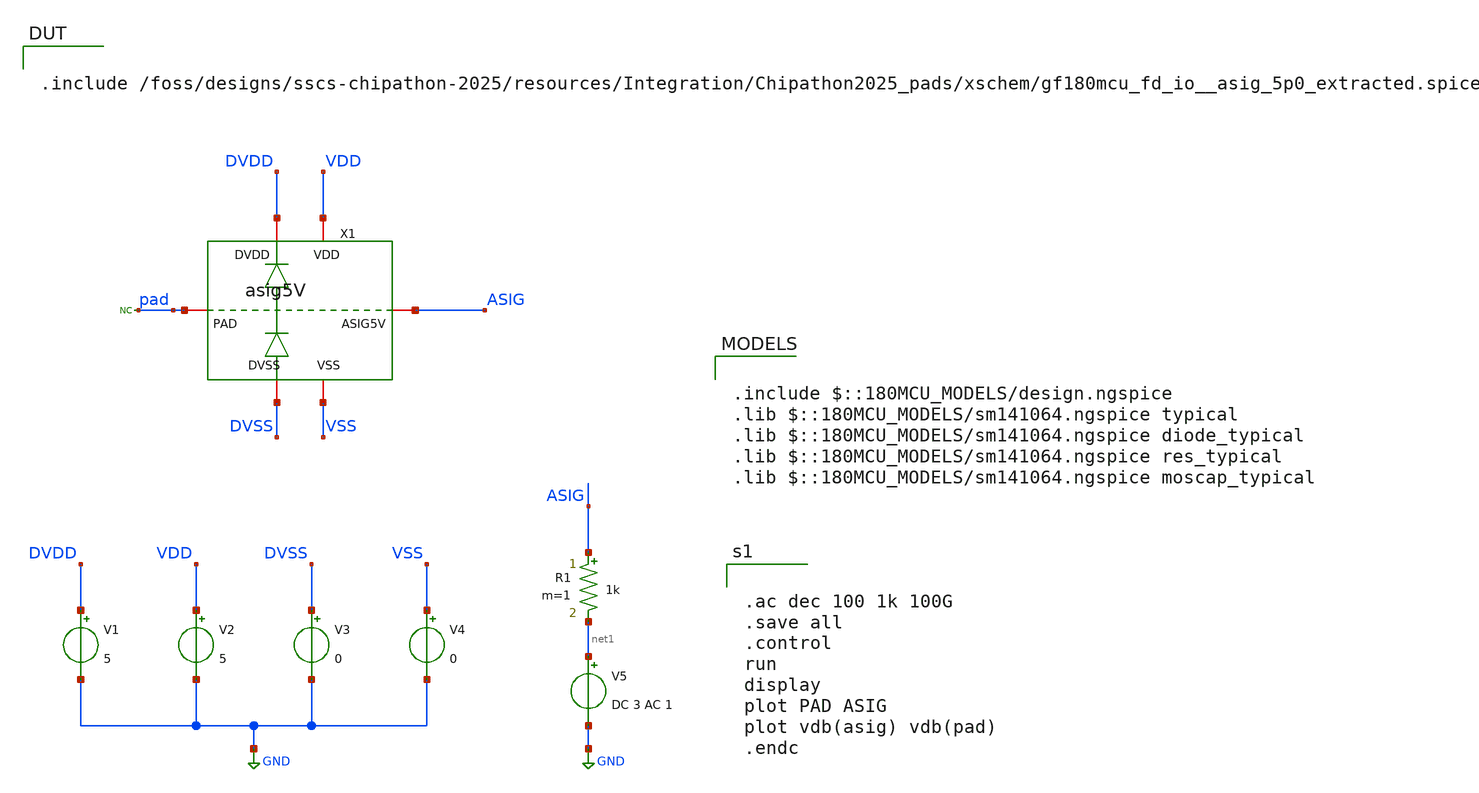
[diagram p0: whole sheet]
** sch_path: examples/pads_simulation/asig5V_AC_symbol_tb.sch
**.subckt asig5V_AC_symbol_tb
V1 DVDD GND 5
V2 VDD GND 5
V3 DVSS GND 0
V4 VSS GND 0
V5 net1 GND DC 3 AC 1
R1 ASIG net1 1k m=1
* noconn pad
X1 DVSS DVDD VSS VDD pad ASIG gf180mcu_fd_io__asig_5p0_extracted
**** begin user architecture code

.include /foss/designs/sscs-chipathon-2025/resources/Integration/Chipathon2025_pads/xschem/gf180mcu_fd_io__asig_5p0_extracted.spice


.include $::180MCU_MODELS/design.ngspice
.lib $::180MCU_MODELS/sm141064.ngspice typical
.lib $::180MCU_MODELS/sm141064.ngspice diode_typical
.lib $::180MCU_MODELS/sm141064.ngspice res_typical
.lib $::180MCU_MODELS/sm141064.ngspice moscap_typical



.ac dec 100 1k 100G
.save all
.control
run
display
plot PAD ASIG
plot vdb(asig) vdb(pad)
.endc


**** end user architecture code
**.ends
.GLOBAL GND
.end
